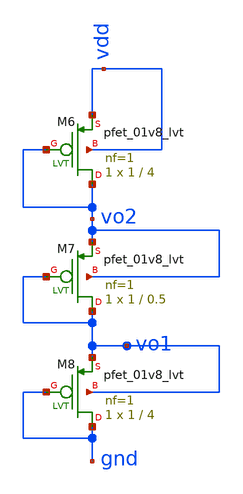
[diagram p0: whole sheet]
** sch_path: xschem/xschemfiles/ref_lvs.sch
**.subckt ref_lvs
XM6 vo2 vo2 vdd vdd sky130_fd_pr__pfet_01v8_lvt L=4 W=1 nf=1 ad='int((nf+1)/2) * W/nf * 0.29' as='int((nf+2)/2) * W/nf * 0.29'
+ pd='2*int((nf+1)/2) * (W/nf + 0.29)' ps='2*int((nf+2)/2) * (W/nf + 0.29)' nrd='0.29 / W' nrs='0.29 / W'
+ sa=0 sb=0 sd=0 mult=1 m=1
XM7 vo1 vo1 vo2 vo2 sky130_fd_pr__pfet_01v8_lvt L=0.5 W=1 nf=1 ad='int((nf+1)/2) * W/nf * 0.29' as='int((nf+2)/2) * W/nf * 0.29'
+ pd='2*int((nf+1)/2) * (W/nf + 0.29)' ps='2*int((nf+2)/2) * (W/nf + 0.29)' nrd='0.29 / W' nrs='0.29 / W'
+ sa=0 sb=0 sd=0 mult=1 m=1
XM8 gnd gnd vo1 vo1 sky130_fd_pr__pfet_01v8_lvt L=4 W=1 nf=1 ad='int((nf+1)/2) * W/nf * 0.29' as='int((nf+2)/2) * W/nf * 0.29'
+ pd='2*int((nf+1)/2) * (W/nf + 0.29)' ps='2*int((nf+2)/2) * (W/nf + 0.29)' nrd='0.29 / W' nrs='0.29 / W'
+ sa=0 sb=0 sd=0 mult=1 m=1
**** begin user architecture code

** opencircuitdesign pdks install
.lib $::SKYWATER_MODELS/sky130.lib.spice tt


**** end user architecture code
**.ends
.end
